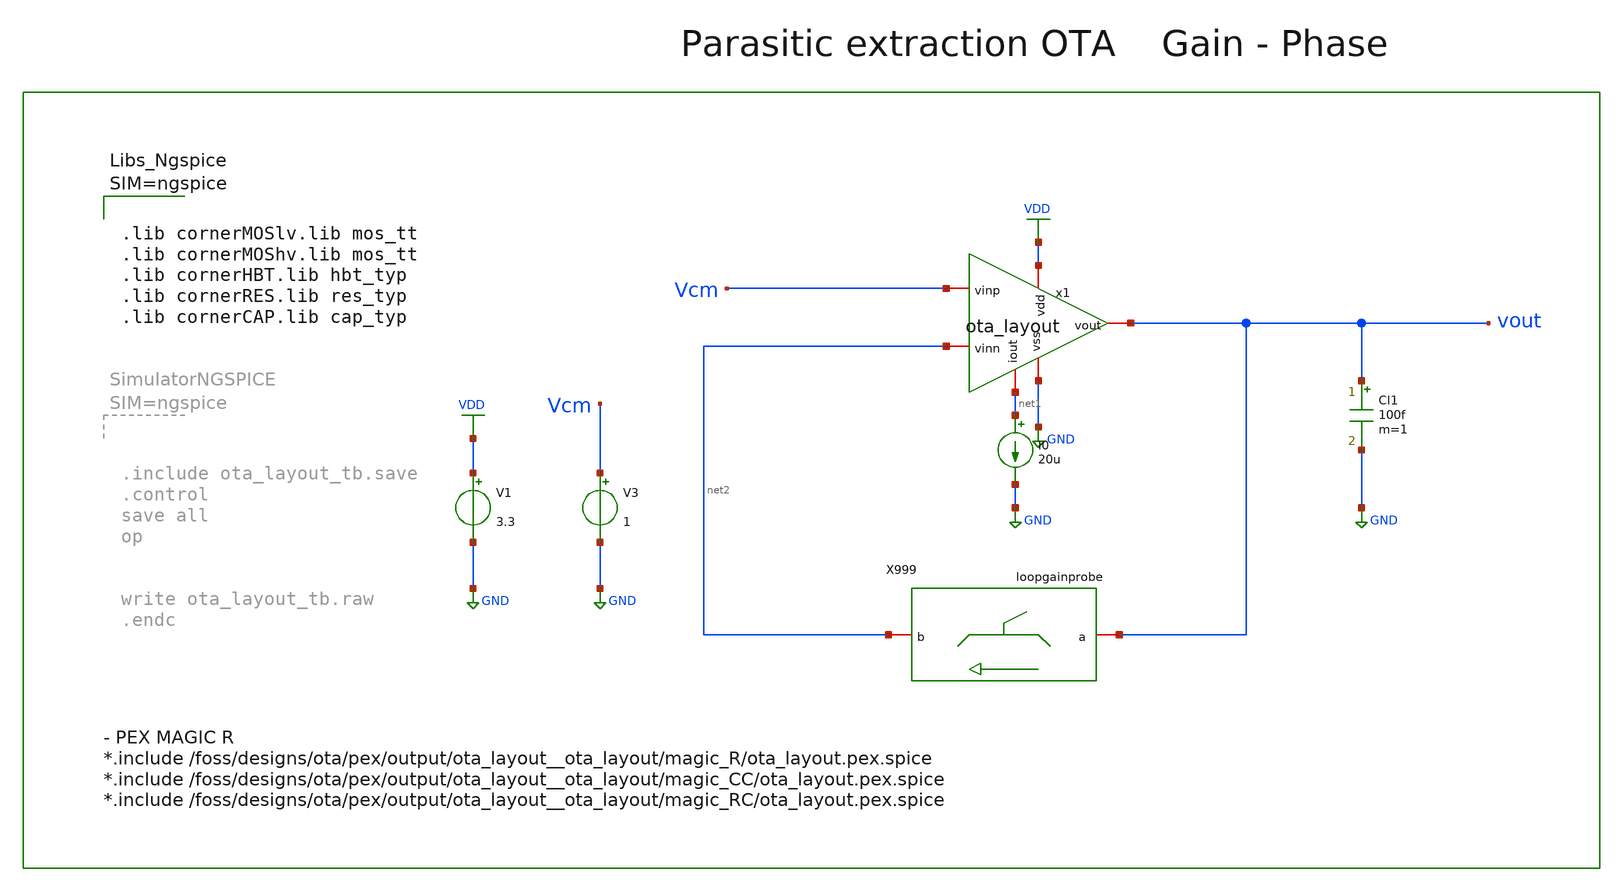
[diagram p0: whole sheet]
** sch_path: dependencies/pmu_ip/dependencies/OTA/OTA-main/netlist/pex/tb/ota_layout_tb.sch
**.subckt ota_layout_tb
I0 net1 GND 20u
V1 VDD GND 3.3
V3 Vcm GND 1
Cl1 vout GND 100f m=1
X999 vout net2 loopgainprobe
x1 VDD GND net1 Vcm net2 vout ota_layout
**** begin user architecture code



.lib cornerMOSlv.lib mos_tt
.lib cornerMOShv.lib mos_tt
.lib cornerHBT.lib hbt_typ
.lib cornerRES.lib res_typ
.lib cornerCAP.lib cap_typ





.include  /foss/designs/designs_/ITI_Analog/Misc/LoopGainProbe/stb.spi
*.include /foss/designs/ota/pex/output/ota_layout__ota_layout/magic_R/ota_layout.pex.spice
*.include /foss/designs/ota/pex/output/ota_layout__ota_layout/magic_CC/ota_layout.pex.spice
.include /foss/designs/ota/pex/output/ota_layout__ota_layout/magic_RC/ota_layout.pex.spice


**** end user architecture code
**.ends
.GLOBAL GND
.GLOBAL VDD
.end
